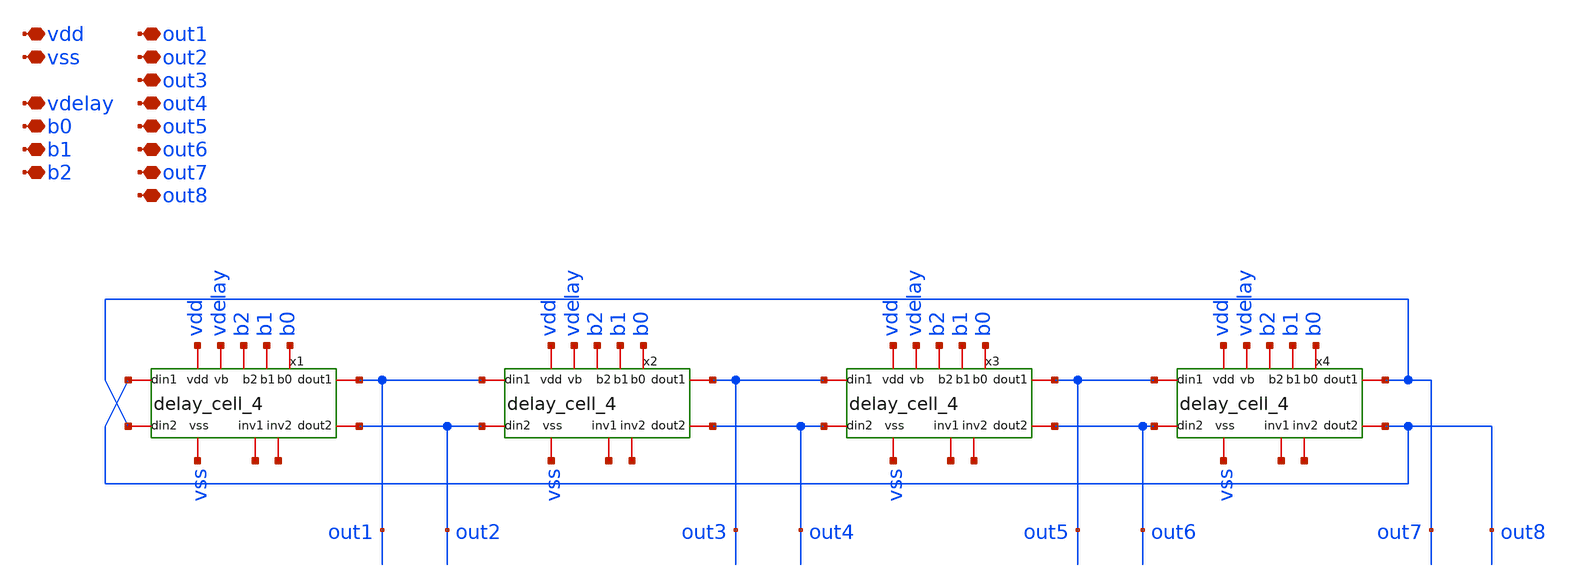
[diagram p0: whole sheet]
** sch_path: xschem/vco_core_8.sch
**.subckt vco_core_8 vdd vss vdelay b0 b1 b2 out1 out2 out3 out4 out5 out6 out7 out8
*.iopin vdd
*.iopin vss
*.iopin vdelay
*.iopin b0
*.iopin b1
*.iopin b2
*.iopin out1
*.iopin out2
*.iopin out3
*.iopin out4
*.iopin out5
*.iopin out6
*.iopin out7
*.iopin out8
x1 vdd vdelay out2 out1 out7 out8 vss b2 b1 b0 net1 net2 delay_cell_4
x2 vdd vdelay out4 out3 out2 out1 vss b2 b1 b0 net3 net4 delay_cell_4
x3 vdd vdelay out6 out5 out4 out3 vss b2 b1 b0 net5 net6 delay_cell_4
x4 vdd vdelay out8 out7 out6 out5 vss b2 b1 b0 net7 net8 delay_cell_4
**.ends
.end
